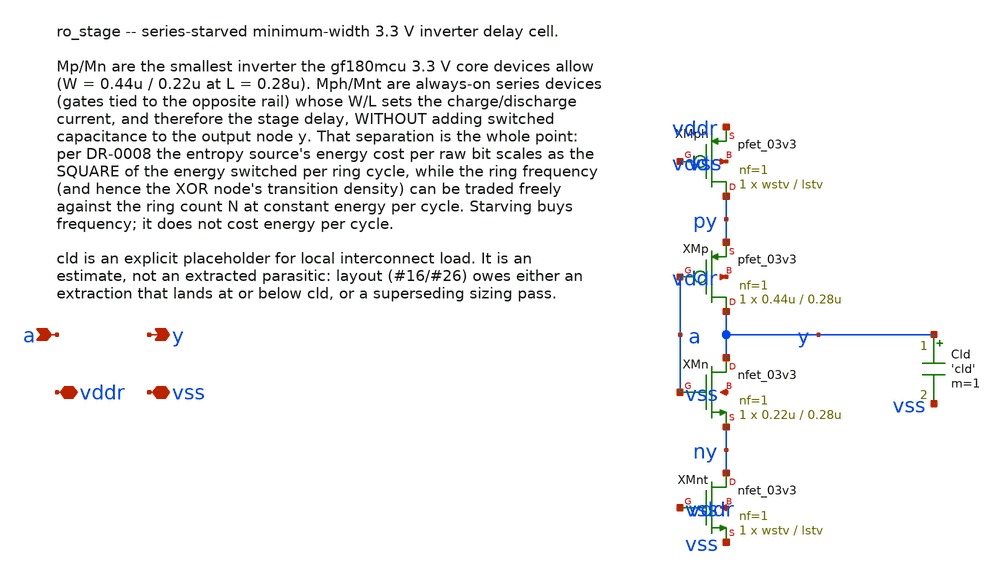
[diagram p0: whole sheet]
** sch_path: design/xschem/ro_stage.sch
**.subckt ro_stage a y vddr vss
*.ipin a
*.opin y
*.iopin vddr
*.iopin vss
XMph py vss vddr vddr pfet_03v3 L=lstv W=wstv nf=1 ad='int((nf+1)/2) * W/nf * 0.18u' as='int((nf+2)/2) * W/nf * 0.18u'
+ pd='2*int((nf+1)/2) * (W/nf + 0.18u)' ps='2*int((nf+2)/2) * (W/nf + 0.18u)' nrd='0.18u / W' nrs='0.18u / W'
+ sa=0 sb=0 sd=0 m=1
XMp y a py vddr pfet_03v3 L=0.28u W=0.44u nf=1 ad='int((nf+1)/2) * W/nf * 0.18u' as='int((nf+2)/2) * W/nf * 0.18u'
+ pd='2*int((nf+1)/2) * (W/nf + 0.18u)' ps='2*int((nf+2)/2) * (W/nf + 0.18u)' nrd='0.18u / W' nrs='0.18u / W'
+ sa=0 sb=0 sd=0 m=1
XMn y a ny vss nfet_03v3 L=0.28u W=0.22u nf=1 ad='int((nf+1)/2) * W/nf * 0.18u' as='int((nf+2)/2) * W/nf * 0.18u'
+ pd='2*int((nf+1)/2) * (W/nf + 0.18u)' ps='2*int((nf+2)/2) * (W/nf + 0.18u)' nrd='0.18u / W' nrs='0.18u / W'
+ sa=0 sb=0 sd=0 m=1
XMnt ny vddr vss vss nfet_03v3 L=lstv W=wstv nf=1 ad='int((nf+1)/2) * W/nf * 0.18u' as='int((nf+2)/2) * W/nf * 0.18u'
+ pd='2*int((nf+1)/2) * (W/nf + 0.18u)' ps='2*int((nf+2)/2) * (W/nf + 0.18u)' nrd='0.18u / W' nrs='0.18u / W'
+ sa=0 sb=0 sd=0 m=1
Cld y vss 'cld' m=1
**.ends
.end
